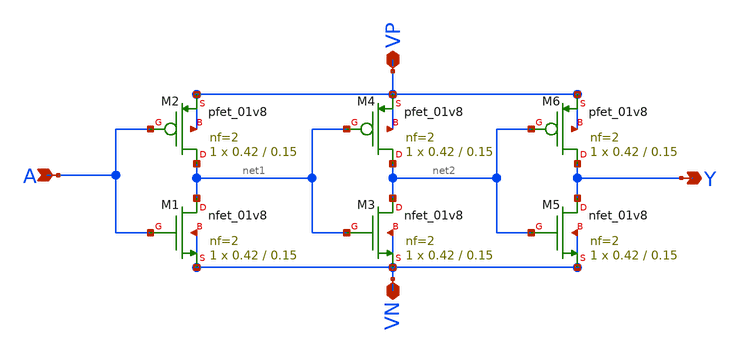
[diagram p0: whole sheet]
** sch_path: week 3/sim/1/3_stage_RO.sch
**.subckt 3_stage_RO A Y VN VP
*.ipin A
*.opin Y
*.iopin VN
*.iopin VP
XM1 net1 A VN VN sky130_fd_pr__nfet_01v8 L=0.15 W=0.42 nf=2 ad='int((nf+1)/2) * W/nf * 0.29' as='int((nf+2)/2) * W/nf * 0.29'
+ pd='2*int((nf+1)/2) * (W/nf + 0.29)' ps='2*int((nf+2)/2) * (W/nf + 0.29)' nrd='0.29 / W' nrs='0.29 / W'
+ sa=0 sb=0 sd=0 mult=1 m=1
XM2 net1 A VP VP sky130_fd_pr__pfet_01v8 L=0.15 W=0.42 nf=2 ad='int((nf+1)/2) * W/nf * 0.29' as='int((nf+2)/2) * W/nf * 0.29'
+ pd='2*int((nf+1)/2) * (W/nf + 0.29)' ps='2*int((nf+2)/2) * (W/nf + 0.29)' nrd='0.29 / W' nrs='0.29 / W'
+ sa=0 sb=0 sd=0 mult=1 m=1
XM3 net2 net1 VN VN sky130_fd_pr__nfet_01v8 L=0.15 W=0.42 nf=2 ad='int((nf+1)/2) * W/nf * 0.29' as='int((nf+2)/2) * W/nf * 0.29'
+ pd='2*int((nf+1)/2) * (W/nf + 0.29)' ps='2*int((nf+2)/2) * (W/nf + 0.29)' nrd='0.29 / W' nrs='0.29 / W'
+ sa=0 sb=0 sd=0 mult=1 m=1
XM4 net2 net1 VP VP sky130_fd_pr__pfet_01v8 L=0.15 W=0.42 nf=2 ad='int((nf+1)/2) * W/nf * 0.29' as='int((nf+2)/2) * W/nf * 0.29'
+ pd='2*int((nf+1)/2) * (W/nf + 0.29)' ps='2*int((nf+2)/2) * (W/nf + 0.29)' nrd='0.29 / W' nrs='0.29 / W'
+ sa=0 sb=0 sd=0 mult=1 m=1
XM5 Y net2 VN VN sky130_fd_pr__nfet_01v8 L=0.15 W=0.42 nf=2 ad='int((nf+1)/2) * W/nf * 0.29' as='int((nf+2)/2) * W/nf * 0.29'
+ pd='2*int((nf+1)/2) * (W/nf + 0.29)' ps='2*int((nf+2)/2) * (W/nf + 0.29)' nrd='0.29 / W' nrs='0.29 / W'
+ sa=0 sb=0 sd=0 mult=1 m=1
XM6 Y net2 VP VP sky130_fd_pr__pfet_01v8 L=0.15 W=0.42 nf=2 ad='int((nf+1)/2) * W/nf * 0.29' as='int((nf+2)/2) * W/nf * 0.29'
+ pd='2*int((nf+1)/2) * (W/nf + 0.29)' ps='2*int((nf+2)/2) * (W/nf + 0.29)' nrd='0.29 / W' nrs='0.29 / W'
+ sa=0 sb=0 sd=0 mult=1 m=1
**.ends
.end
